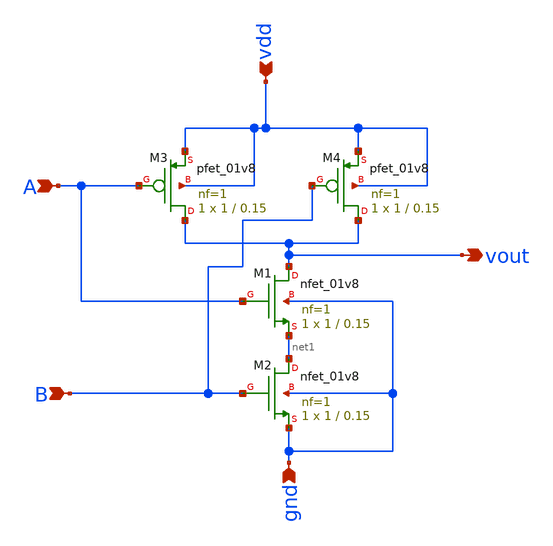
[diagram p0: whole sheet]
** sch_path: nand.sch
**.subckt nand A B gnd vdd vout
*.ipin A
*.ipin B
*.ipin gnd
*.ipin vdd
*.opin vout
XM1 vout A net1 gnd sky130_fd_pr__nfet_01v8 L=0.15 W=1 nf=1 ad='int((nf+1)/2) * W/nf * 0.29' as='int((nf+2)/2) * W/nf * 0.29'
+ pd='2*int((nf+1)/2) * (W/nf + 0.29)' ps='2*int((nf+2)/2) * (W/nf + 0.29)' nrd='0.29 / W' nrs='0.29 / W'
+ sa=0 sb=0 sd=0 mult=1 m=1
XM2 net1 B gnd gnd sky130_fd_pr__nfet_01v8 L=0.15 W=1 nf=1 ad='int((nf+1)/2) * W/nf * 0.29' as='int((nf+2)/2) * W/nf * 0.29'
+ pd='2*int((nf+1)/2) * (W/nf + 0.29)' ps='2*int((nf+2)/2) * (W/nf + 0.29)' nrd='0.29 / W' nrs='0.29 / W'
+ sa=0 sb=0 sd=0 mult=1 m=1
XM3 vout A vdd vdd sky130_fd_pr__pfet_01v8 L=0.15 W=1 nf=1 ad='int((nf+1)/2) * W/nf * 0.29' as='int((nf+2)/2) * W/nf * 0.29'
+ pd='2*int((nf+1)/2) * (W/nf + 0.29)' ps='2*int((nf+2)/2) * (W/nf + 0.29)' nrd='0.29 / W' nrs='0.29 / W'
+ sa=0 sb=0 sd=0 mult=1 m=1
XM4 vout B vdd vdd sky130_fd_pr__pfet_01v8 L=0.15 W=1 nf=1 ad='int((nf+1)/2) * W/nf * 0.29' as='int((nf+2)/2) * W/nf * 0.29'
+ pd='2*int((nf+1)/2) * (W/nf + 0.29)' ps='2*int((nf+2)/2) * (W/nf + 0.29)' nrd='0.29 / W' nrs='0.29 / W'
+ sa=0 sb=0 sd=0 mult=1 m=1
**.ends
.end
